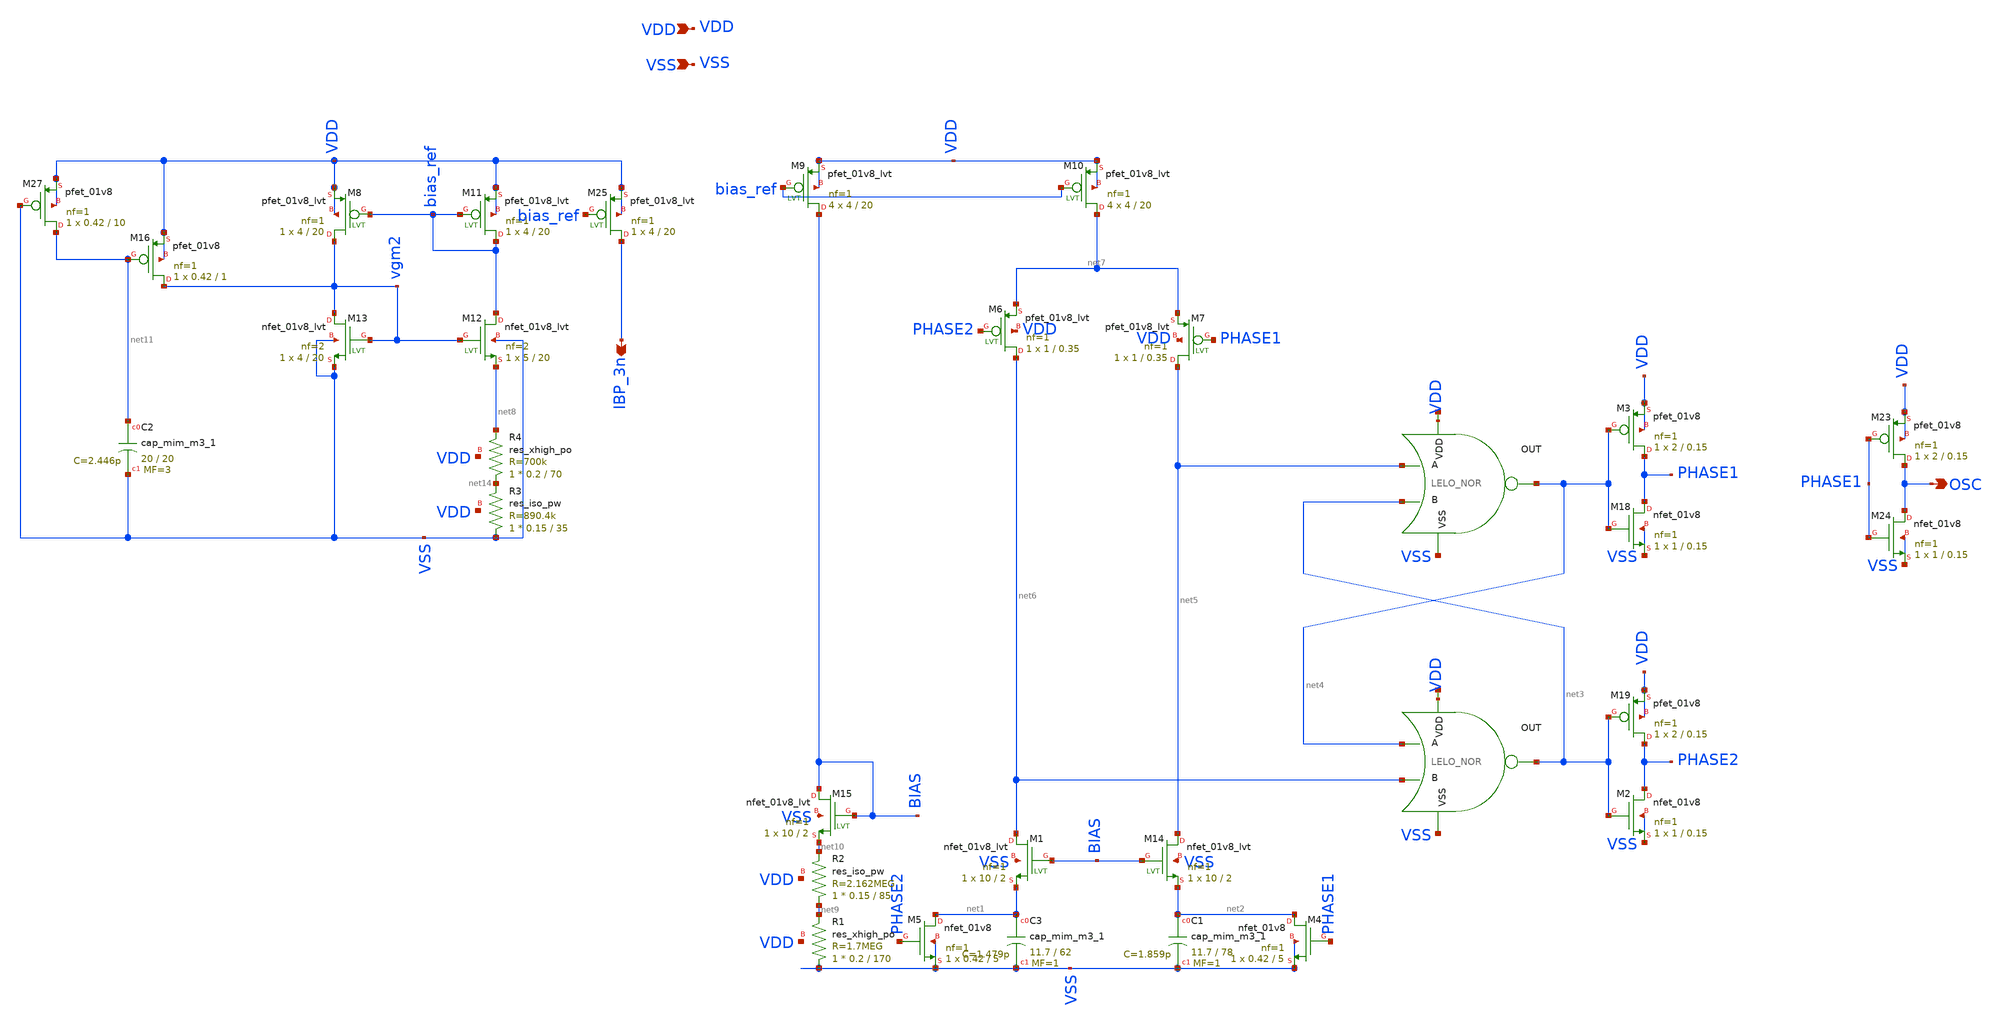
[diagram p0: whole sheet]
** sch_path: design/LELO_SVOD_SKY130A/LELO_SVOD_RELOSC.sch
**.subckt LELO_SVOD_RELOSC VDD VSS OSC IBP_3n
*.ipin VDD
*.ipin VSS
*.opin OSC
*.opin IBP_3n
x1 net12 net4 net5 net3 VSS LELO_NOR
x2 net13 net3 net4 net6 VSS LELO_NOR
XM6 net6 PHASE2 net7 VDD sky130_fd_pr__pfet_01v8_lvt L=0.35 W=1 nf=1 ad='int((1 + 1)/2) * 1 / 1 * 0.29'
+ as='int((1 + 2)/2) * 1 / 1 * 0.29' pd='2*int((1 + 1)/2) * (1 / 1 + 0.29)' ps='2*int((1 + 2)/2) * (1 / 1 + 0.29)'
+ nrd='0.29 / 1 ' nrs='0.29 / 1 ' sa=0 sb=0 sd=0 mult=1 m=1
XM7 net5 PHASE1 net7 VDD sky130_fd_pr__pfet_01v8_lvt L=0.35 W=1 nf=1 ad='int((1 + 1)/2) * 1 / 1 * 0.29'
+ as='int((1 + 2)/2) * 1 / 1 * 0.29' pd='2*int((1 + 1)/2) * (1 / 1 + 0.29)' ps='2*int((1 + 2)/2) * (1 / 1 + 0.29)'
+ nrd='0.29 / 1 ' nrs='0.29 / 1 ' sa=0 sb=0 sd=0 mult=1 m=1
XM11 bias_ref bias_ref VDD VDD sky130_fd_pr__pfet_01v8_lvt L=20 W=4 nf=1 ad='int((1 + 1)/2) * 4 / 1 * 0.29'
+ as='int((1 + 2)/2) * 4 / 1 * 0.29' pd='2*int((1 + 1)/2) * (4 / 1 + 0.29)' ps='2*int((1 + 2)/2) * (4 / 1 + 0.29)'
+ nrd='0.29 / 4 ' nrs='0.29 / 4 ' sa=0 sb=0 sd=0 mult=1 m=1
XC3 net1 VSS sky130_fd_pr__cap_mim_m3_1 W=11.7 L=62 MF=1 m=1
XC1 net2 VSS sky130_fd_pr__cap_mim_m3_1 W=11.7 L=78 MF=1 m=1
XM4 net2 PHASE1 VSS VSS sky130_fd_pr__nfet_01v8 L=5 W=0.42 nf=1 ad='int((1 + 1)/2) * 0.42 / 1 * 0.29'
+ as='int((1 + 2)/2) * 0.42 / 1 * 0.29' pd='2*int((1 + 1)/2) * (0.42 / 1 + 0.29)' ps='2*int((1 + 2)/2) * (0.42 / 1 + 0.29)'
+ nrd='0.29 / 0.42 ' nrs='0.29 / 0.42 ' sa=0 sb=0 sd=0 mult=1 m=1
XM5 net1 PHASE2 VSS VSS sky130_fd_pr__nfet_01v8 L=5 W=0.42 nf=1 ad='int((1 + 1)/2) * 0.42 / 1 * 0.29'
+ as='int((1 + 2)/2) * 0.42 / 1 * 0.29' pd='2*int((1 + 1)/2) * (0.42 / 1 + 0.29)' ps='2*int((1 + 2)/2) * (0.42 / 1 + 0.29)'
+ nrd='0.29 / 0.42 ' nrs='0.29 / 0.42 ' sa=0 sb=0 sd=0 mult=1 m=1
XM1 net6 BIAS net1 VSS sky130_fd_pr__nfet_01v8_lvt L=2 W=10 nf=1 ad='int((1 + 1)/2) * 10 / 1 * 0.29'
+ as='int((1 + 2)/2) * 10 / 1 * 0.29' pd='2*int((1 + 1)/2) * (10 / 1 + 0.29)' ps='2*int((1 + 2)/2) * (10 / 1 + 0.29)'
+ nrd='0.29 / 10 ' nrs='0.29 / 10 ' sa=0 sb=0 sd=0 mult=1 m=1
XM8 vgm2 bias_ref VDD VDD sky130_fd_pr__pfet_01v8_lvt L=20 W=4 nf=1 ad='int((1 + 1)/2) * 4 / 1 * 0.29'
+ as='int((1 + 2)/2) * 4 / 1 * 0.29' pd='2*int((1 + 1)/2) * (4 / 1 + 0.29)' ps='2*int((1 + 2)/2) * (4 / 1 + 0.29)'
+ nrd='0.29 / 4 ' nrs='0.29 / 4 ' sa=0 sb=0 sd=0 mult=1 m=1
XM12 bias_ref vgm2 net8 VSS sky130_fd_pr__nfet_01v8_lvt L=20 W=5 nf=2 ad='int((2 + 1)/2) * 5 / 2 * 0.29'
+ as='int((2 + 2)/2) * 5 / 2 * 0.29' pd='2*int((2 + 1)/2) * (5 / 2 + 0.29)' ps='2*int((2 + 2)/2) * (5 / 2 + 0.29)'
+ nrd='0.29 / 5 ' nrs='0.29 / 5 ' sa=0 sb=0 sd=0 mult=1 m=1
XM13 vgm2 vgm2 VSS VSS sky130_fd_pr__nfet_01v8_lvt L=20 W=4 nf=2 ad='int((2 + 1)/2) * 4 / 2 * 0.29' as='int((2 + 2)/2) * 4 / 2 * 0.29'
+ pd='2*int((2 + 1)/2) * (4 / 2 + 0.29)' ps='2*int((2 + 2)/2) * (4 / 2 + 0.29)' nrd='0.29 / 4 ' nrs='0.29 / 4 '
+ sa=0 sb=0 sd=0 mult=1 m=1
XM9 BIAS bias_ref VDD VDD sky130_fd_pr__pfet_01v8_lvt L=20 W=4 nf=1 ad='int((1 + 1)/2) * 4 / 1 * 0.29'
+ as='int((1 + 2)/2) * 4 / 1 * 0.29' pd='2*int((1 + 1)/2) * (4 / 1 + 0.29)' ps='2*int((1 + 2)/2) * (4 / 1 + 0.29)'
+ nrd='0.29 / 4 ' nrs='0.29 / 4 ' sa=0 sb=0 sd=0 mult=4 m=4
XM10 net7 bias_ref VDD VDD sky130_fd_pr__pfet_01v8_lvt L=20 W=4 nf=1 ad='int((1 + 1)/2) * 4 / 1 * 0.29'
+ as='int((1 + 2)/2) * 4 / 1 * 0.29' pd='2*int((1 + 1)/2) * (4 / 1 + 0.29)' ps='2*int((1 + 2)/2) * (4 / 1 + 0.29)'
+ nrd='0.29 / 4 ' nrs='0.29 / 4 ' sa=0 sb=0 sd=0 mult=4 m=4
XM14 net5 BIAS net2 VSS sky130_fd_pr__nfet_01v8_lvt L=2 W=10 nf=1 ad='int((1 + 1)/2) * 10 / 1 * 0.29'
+ as='int((1 + 2)/2) * 10 / 1 * 0.29' pd='2*int((1 + 1)/2) * (10 / 1 + 0.29)' ps='2*int((1 + 2)/2) * (10 / 1 + 0.29)'
+ nrd='0.29 / 10 ' nrs='0.29 / 10 ' sa=0 sb=0 sd=0 mult=1 m=1
XM15 BIAS BIAS net10 VSS sky130_fd_pr__nfet_01v8_lvt L=2 W=10 nf=1 ad='int((1 + 1)/2) * 10 / 1 * 0.29'
+ as='int((1 + 2)/2) * 10 / 1 * 0.29' pd='2*int((1 + 1)/2) * (10 / 1 + 0.29)' ps='2*int((1 + 2)/2) * (10 / 1 + 0.29)'
+ nrd='0.29 / 10 ' nrs='0.29 / 10 ' sa=0 sb=0 sd=0 mult=1 m=1
XR3 VSS net14 VDD sky130_fd_pr__res_iso_pw W=0.15 L=35 m=1
XR1 VSS net9 VDD sky130_fd_pr__res_xhigh_po W=0.2 L=170 mult=1 m=1
XR2 net9 net10 VDD sky130_fd_pr__res_iso_pw W=0.15 L=85 m=1
XM2 PHASE2 net3 VSS VSS sky130_fd_pr__nfet_01v8 L=0.15 W=1 nf=1 ad='int((1 + 1)/2) * 1 / 1 * 0.29' as='int((1 + 2)/2) * 1 / 1 * 0.29'
+ pd='2*int((1 + 1)/2) * (1 / 1 + 0.29)' ps='2*int((1 + 2)/2) * (1 / 1 + 0.29)' nrd='0.29 / 1 ' nrs='0.29 / 1 '
+ sa=0 sb=0 sd=0 mult=1 m=1
XM18 PHASE1 net4 VSS VSS sky130_fd_pr__nfet_01v8 L=0.15 W=1 nf=1 ad='int((1 + 1)/2) * 1 / 1 * 0.29' as='int((1 + 2)/2) * 1 / 1 * 0.29'
+ pd='2*int((1 + 1)/2) * (1 / 1 + 0.29)' ps='2*int((1 + 2)/2) * (1 / 1 + 0.29)' nrd='0.29 / 1 ' nrs='0.29 / 1 '
+ sa=0 sb=0 sd=0 mult=1 m=1
XM24 OSC PHASE1 VSS VSS sky130_fd_pr__nfet_01v8 L=0.15 W=1 nf=1 ad='int((1 + 1)/2) * 1 / 1 * 0.29' as='int((1 + 2)/2) * 1 / 1 * 0.29'
+ pd='2*int((1 + 1)/2) * (1 / 1 + 0.29)' ps='2*int((1 + 2)/2) * (1 / 1 + 0.29)' nrd='0.29 / 1 ' nrs='0.29 / 1 '
+ sa=0 sb=0 sd=0 mult=1 m=1
XM25 IBP_3n bias_ref VDD VDD sky130_fd_pr__pfet_01v8_lvt L=20 W=4 nf=1 ad='int((1 + 1)/2) * 4 / 1 * 0.29'
+ as='int((1 + 2)/2) * 4 / 1 * 0.29' pd='2*int((1 + 1)/2) * (4 / 1 + 0.29)' ps='2*int((1 + 2)/2) * (4 / 1 + 0.29)'
+ nrd='0.29 / 4 ' nrs='0.29 / 4 ' sa=0 sb=0 sd=0 mult=1 m=1
XM16 vgm2 net11 VDD VDD sky130_fd_pr__pfet_01v8 L=1 W=0.42 nf=1 ad='int((1 + 1)/2) * 0.42 / 1 * 0.29'
+ as='int((1 + 2)/2) * 0.42 / 1 * 0.29' pd='2*int((1 + 1)/2) * (0.42 / 1 + 0.29)' ps='2*int((1 + 2)/2) * (0.42 / 1 + 0.29)'
+ nrd='0.29 / 0.42 ' nrs='0.29 / 0.42 ' sa=0 sb=0 sd=0 mult=1 m=1
XM27 net11 VSS VDD VDD sky130_fd_pr__pfet_01v8 L=10 W=0.42 nf=1 ad='int((1 + 1)/2) * 0.42 / 1 * 0.29'
+ as='int((1 + 2)/2) * 0.42 / 1 * 0.29' pd='2*int((1 + 1)/2) * (0.42 / 1 + 0.29)' ps='2*int((1 + 2)/2) * (0.42 / 1 + 0.29)'
+ nrd='0.29 / 0.42 ' nrs='0.29 / 0.42 ' sa=0 sb=0 sd=0 mult=1 m=1
XC2 net11 VSS sky130_fd_pr__cap_mim_m3_1 W=20 L=20 MF=3 m=3
XM23 OSC PHASE1 VDD VDD sky130_fd_pr__pfet_01v8 L=0.15 W=2 nf=1 ad='int((1 + 1)/2) * 2 / 1 * 0.29' as='int((1 + 2)/2) * 2 / 1 * 0.29'
+ pd='2*int((1 + 1)/2) * (2 / 1 + 0.29)' ps='2*int((1 + 2)/2) * (2 / 1 + 0.29)' nrd='0.29 / 2 ' nrs='0.29 / 2 '
+ sa=0 sb=0 sd=0 mult=1 m=1
XM3 PHASE1 net4 VDD VDD sky130_fd_pr__pfet_01v8 L=0.15 W=2 nf=1 ad='int((1 + 1)/2) * 2 / 1 * 0.29' as='int((1 + 2)/2) * 2 / 1 * 0.29'
+ pd='2*int((1 + 1)/2) * (2 / 1 + 0.29)' ps='2*int((1 + 2)/2) * (2 / 1 + 0.29)' nrd='0.29 / 2 ' nrs='0.29 / 2 '
+ sa=0 sb=0 sd=0 mult=1 m=1
XM19 PHASE2 net3 VDD VDD sky130_fd_pr__pfet_01v8 L=0.15 W=2 nf=1 ad='int((1 + 1)/2) * 2 / 1 * 0.29' as='int((1 + 2)/2) * 2 / 1 * 0.29'
+ pd='2*int((1 + 1)/2) * (2 / 1 + 0.29)' ps='2*int((1 + 2)/2) * (2 / 1 + 0.29)' nrd='0.29 / 2 ' nrs='0.29 / 2 '
+ sa=0 sb=0 sd=0 mult=1 m=1
XR4 net14 net8 VDD sky130_fd_pr__res_xhigh_po W=0.2 L=70 mult=1 m=1
**.ends

* expanding   symbol:  LELO_SVOD_SKY130A/LELO_NOR.sym # of pins=5
** sym_path: design/LELO_SVOD_SKY130A/LELO_NOR.sym
** sch_path: design/LELO_SVOD_SKY130A/LELO_NOR.sch
.subckt LELO_NOR VDD OUT A B VSS
*.ipin VDD
*.ipin VSS
*.opin OUT
*.ipin A
*.ipin B
XM2 OUT B VSS VSS sky130_fd_pr__nfet_01v8 L=0.15 W=2 nf=1 ad='int((1 + 1)/2) * 2 / 1 * 0.29' as='int((1 + 2)/2) * 2 / 1 * 0.29'
+ pd='2*int((1 + 1)/2) * (2 / 1 + 0.29)' ps='2*int((1 + 2)/2) * (2 / 1 + 0.29)' nrd='0.29 / 2 ' nrs='0.29 / 2 '
+ sa=0 sb=0 sd=0 mult=1 m=1
XM1 OUT A VSS VSS sky130_fd_pr__nfet_01v8 L=0.15 W=2 nf=1 ad='int((1 + 1)/2) * 2 / 1 * 0.29' as='int((1 + 2)/2) * 2 / 1 * 0.29'
+ pd='2*int((1 + 1)/2) * (2 / 1 + 0.29)' ps='2*int((1 + 2)/2) * (2 / 1 + 0.29)' nrd='0.29 / 2 ' nrs='0.29 / 2 '
+ sa=0 sb=0 sd=0 mult=1 m=1
XM3 OUT B net1 VDD sky130_fd_pr__pfet_01v8 L=0.15 W=4 nf=1 ad='int((1 + 1)/2) * 4 / 1 * 0.29' as='int((1 + 2)/2) * 4 / 1 * 0.29'
+ pd='2*int((1 + 1)/2) * (4 / 1 + 0.29)' ps='2*int((1 + 2)/2) * (4 / 1 + 0.29)' nrd='0.29 / 4 ' nrs='0.29 / 4 '
+ sa=0 sb=0 sd=0 mult=1 m=1
XM4 net1 A VDD VDD sky130_fd_pr__pfet_01v8 L=0.15 W=4 nf=1 ad='int((1 + 1)/2) * 4 / 1 * 0.29' as='int((1 + 2)/2) * 4 / 1 * 0.29'
+ pd='2*int((1 + 1)/2) * (4 / 1 + 0.29)' ps='2*int((1 + 2)/2) * (4 / 1 + 0.29)' nrd='0.29 / 4 ' nrs='0.29 / 4 '
+ sa=0 sb=0 sd=0 mult=1 m=1
.ends

.end
